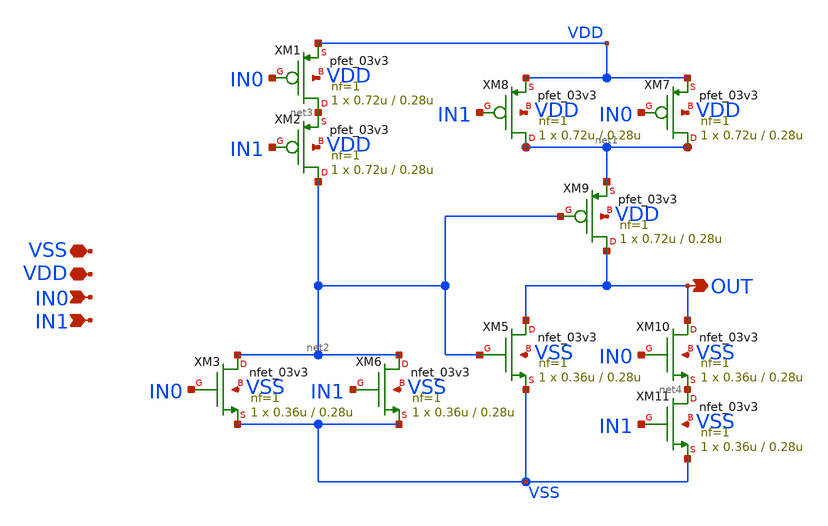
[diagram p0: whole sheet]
** sch_path: CAD4/xor2.sch
**.subckt xor2 VSS VDD IN0 IN1 OUT
*.iopin VSS
*.iopin VDD
*.ipin IN0
*.ipin IN1
*.opin OUT
XM1 net3 IN0 VDD VDD pfet_03v3 L=0.28u W=0.72u nf=1 ad='int((nf+1)/2) * W/nf * 0.18u' as='int((nf+2)/2) * W/nf * 0.18u'
+ pd='2*int((nf+1)/2) * (W/nf + 0.18u)' ps='2*int((nf+2)/2) * (W/nf + 0.18u)' nrd='0.18u / W' nrs='0.18u / W'
+ sa=0 sb=0 sd=0 m=1
XM2 net2 IN1 net3 VDD pfet_03v3 L=0.28u W=0.72u nf=1 ad='int((nf+1)/2) * W/nf * 0.18u' as='int((nf+2)/2) * W/nf * 0.18u'
+ pd='2*int((nf+1)/2) * (W/nf + 0.18u)' ps='2*int((nf+2)/2) * (W/nf + 0.18u)' nrd='0.18u / W' nrs='0.18u / W'
+ sa=0 sb=0 sd=0 m=1
XM3 net2 IN0 VSS VSS nfet_03v3 L=0.28u W=0.36u nf=1 ad='int((nf+1)/2) * W/nf * 0.18u' as='int((nf+2)/2) * W/nf * 0.18u'
+ pd='2*int((nf+1)/2) * (W/nf + 0.18u)' ps='2*int((nf+2)/2) * (W/nf + 0.18u)' nrd='0.18u / W' nrs='0.18u / W'
+ sa=0 sb=0 sd=0 m=1
XM5 OUT net2 VSS VSS nfet_03v3 L=0.28u W=0.36u nf=1 ad='int((nf+1)/2) * W/nf * 0.18u' as='int((nf+2)/2) * W/nf * 0.18u'
+ pd='2*int((nf+1)/2) * (W/nf + 0.18u)' ps='2*int((nf+2)/2) * (W/nf + 0.18u)' nrd='0.18u / W' nrs='0.18u / W'
+ sa=0 sb=0 sd=0 m=1
XM6 net2 IN1 VSS VSS nfet_03v3 L=0.28u W=0.36u nf=1 ad='int((nf+1)/2) * W/nf * 0.18u' as='int((nf+2)/2) * W/nf * 0.18u'
+ pd='2*int((nf+1)/2) * (W/nf + 0.18u)' ps='2*int((nf+2)/2) * (W/nf + 0.18u)' nrd='0.18u / W' nrs='0.18u / W'
+ sa=0 sb=0 sd=0 m=1
XM7 net1 IN0 VDD VDD pfet_03v3 L=0.28u W=0.72u nf=1 ad='int((nf+1)/2) * W/nf * 0.18u' as='int((nf+2)/2) * W/nf * 0.18u'
+ pd='2*int((nf+1)/2) * (W/nf + 0.18u)' ps='2*int((nf+2)/2) * (W/nf + 0.18u)' nrd='0.18u / W' nrs='0.18u / W'
+ sa=0 sb=0 sd=0 m=1
XM8 net1 IN1 VDD VDD pfet_03v3 L=0.28u W=0.72u nf=1 ad='int((nf+1)/2) * W/nf * 0.18u' as='int((nf+2)/2) * W/nf * 0.18u'
+ pd='2*int((nf+1)/2) * (W/nf + 0.18u)' ps='2*int((nf+2)/2) * (W/nf + 0.18u)' nrd='0.18u / W' nrs='0.18u / W'
+ sa=0 sb=0 sd=0 m=1
XM9 OUT net2 net1 VDD pfet_03v3 L=0.28u W=0.72u nf=1 ad='int((nf+1)/2) * W/nf * 0.18u' as='int((nf+2)/2) * W/nf * 0.18u'
+ pd='2*int((nf+1)/2) * (W/nf + 0.18u)' ps='2*int((nf+2)/2) * (W/nf + 0.18u)' nrd='0.18u / W' nrs='0.18u / W'
+ sa=0 sb=0 sd=0 m=1
XM10 OUT IN0 net4 VSS nfet_03v3 L=0.28u W=0.36u nf=1 ad='int((nf+1)/2) * W/nf * 0.18u' as='int((nf+2)/2) * W/nf * 0.18u'
+ pd='2*int((nf+1)/2) * (W/nf + 0.18u)' ps='2*int((nf+2)/2) * (W/nf + 0.18u)' nrd='0.18u / W' nrs='0.18u / W'
+ sa=0 sb=0 sd=0 m=1
XM11 net4 IN1 VSS VSS nfet_03v3 L=0.28u W=0.36u nf=1 ad='int((nf+1)/2) * W/nf * 0.18u' as='int((nf+2)/2) * W/nf * 0.18u'
+ pd='2*int((nf+1)/2) * (W/nf + 0.18u)' ps='2*int((nf+2)/2) * (W/nf + 0.18u)' nrd='0.18u / W' nrs='0.18u / W'
+ sa=0 sb=0 sd=0 m=1
**.ends
.end
